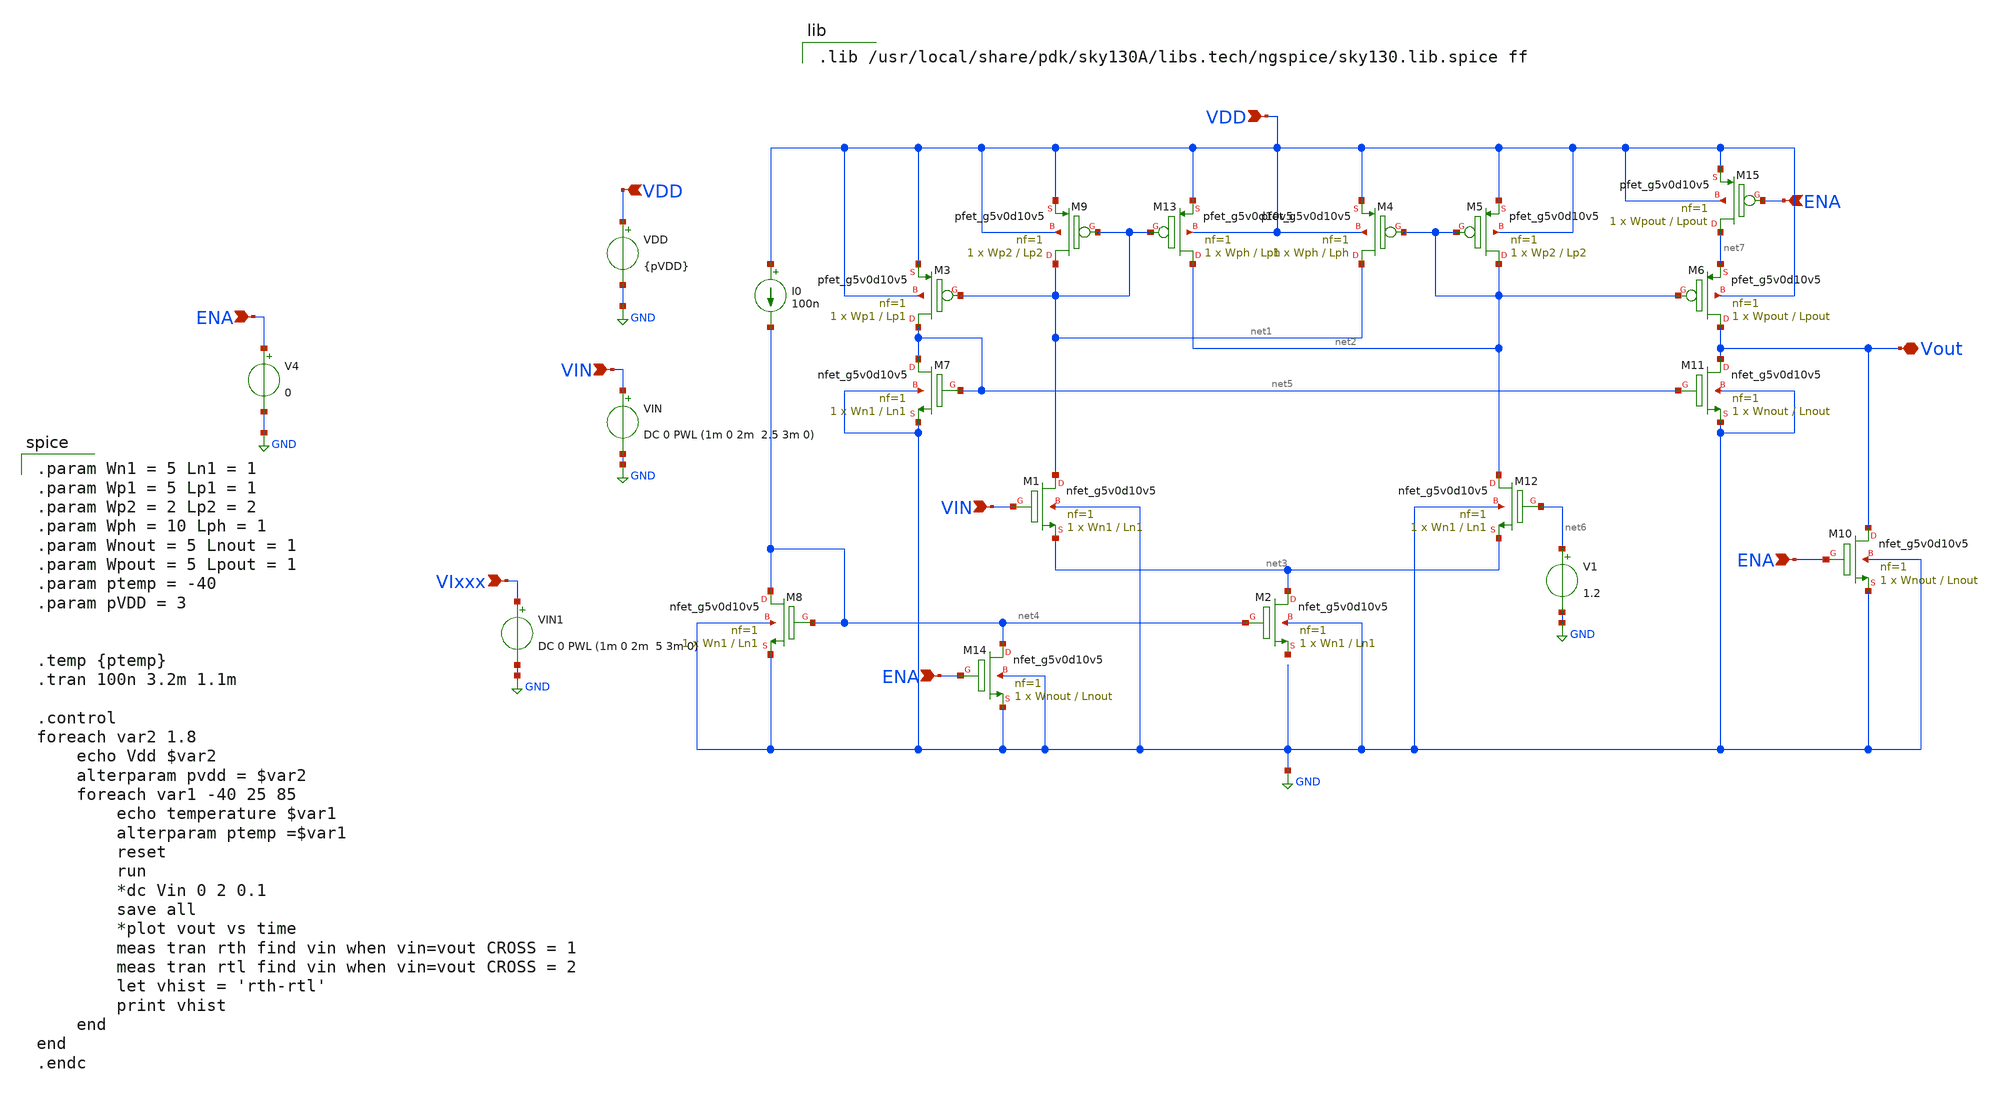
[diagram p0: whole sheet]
** sch_path: xschem/Comparador_Digital_voltage.sch
**.subckt Comparador_Digital_voltage VDD VDD Vout VIN VIN ENA ENA VIxxx ENA ENA
*.ipin VDD
*.ipin VDD
*.iopin Vout
*.ipin VIN
*.ipin VIN
*.ipin ENA
*.ipin ENA
*.ipin VIxxx
*.ipin ENA
*.ipin ENA
V1 net6 GND 1.2
VDD VDD GND {pVDD}
VIN VIN GND DC 0 PWL (1m 0 2m 2.5 3m 0)
I0 VDD net4 100n
XM3 net5 net1 VDD VDD sky130_fd_pr__pfet_g5v0d10v5 L=Lp1 W=Wp1 nf=1 ad='int((nf+1)/2) * W/nf * 0.29'
+ as='int((nf+2)/2) * W/nf * 0.29' pd='2*int((nf+1)/2) * (W/nf + 0.29)' ps='2*int((nf+2)/2) * (W/nf + 0.29)'
+ nrd='0.29 / W' nrs='0.29 / W' sa=0 sb=0 sd=0 mult=1 m=1
XM9 net1 net1 VDD VDD sky130_fd_pr__pfet_g5v0d10v5 L=Lp2 W=Wp2 nf=1 ad='int((nf+1)/2) * W/nf * 0.29'
+ as='int((nf+2)/2) * W/nf * 0.29' pd='2*int((nf+1)/2) * (W/nf + 0.29)' ps='2*int((nf+2)/2) * (W/nf + 0.29)'
+ nrd='0.29 / W' nrs='0.29 / W' sa=0 sb=0 sd=0 mult=1 m=1
XM13 net2 net1 VDD VDD sky130_fd_pr__pfet_g5v0d10v5 L=Lph W=Wph nf=1 ad='int((nf+1)/2) * W/nf * 0.29'
+ as='int((nf+2)/2) * W/nf * 0.29' pd='2*int((nf+1)/2) * (W/nf + 0.29)' ps='2*int((nf+2)/2) * (W/nf + 0.29)'
+ nrd='0.29 / W' nrs='0.29 / W' sa=0 sb=0 sd=0 mult=1 m=1
XM4 net1 net2 VDD VDD sky130_fd_pr__pfet_g5v0d10v5 L=Lph W=Wph nf=1 ad='int((nf+1)/2) * W/nf * 0.29'
+ as='int((nf+2)/2) * W/nf * 0.29' pd='2*int((nf+1)/2) * (W/nf + 0.29)' ps='2*int((nf+2)/2) * (W/nf + 0.29)'
+ nrd='0.29 / W' nrs='0.29 / W' sa=0 sb=0 sd=0 mult=1 m=1
XM5 net2 net2 VDD VDD sky130_fd_pr__pfet_g5v0d10v5 L=Lp2 W=Wp2 nf=1 ad='int((nf+1)/2) * W/nf * 0.29'
+ as='int((nf+2)/2) * W/nf * 0.29' pd='2*int((nf+1)/2) * (W/nf + 0.29)' ps='2*int((nf+2)/2) * (W/nf + 0.29)'
+ nrd='0.29 / W' nrs='0.29 / W' sa=0 sb=0 sd=0 mult=1 m=1
XM6 Vout net2 net7 VDD sky130_fd_pr__pfet_g5v0d10v5 L=Lpout W=Wpout nf=1 ad='int((nf+1)/2) * W/nf * 0.29'
+ as='int((nf+2)/2) * W/nf * 0.29' pd='2*int((nf+1)/2) * (W/nf + 0.29)' ps='2*int((nf+2)/2) * (W/nf + 0.29)'
+ nrd='0.29 / W' nrs='0.29 / W' sa=0 sb=0 sd=0 mult=1 m=1
XM11 Vout net5 GND GND sky130_fd_pr__nfet_g5v0d10v5 L=Lnout W=Wnout nf=1 ad='int((nf+1)/2) * W/nf * 0.29'
+ as='int((nf+2)/2) * W/nf * 0.29' pd='2*int((nf+1)/2) * (W/nf + 0.29)' ps='2*int((nf+2)/2) * (W/nf + 0.29)'
+ nrd='0.29 / W' nrs='0.29 / W' sa=0 sb=0 sd=0 mult=1 m=1
XM12 net2 net6 net3 GND sky130_fd_pr__nfet_g5v0d10v5 L=Ln1 W=Wn1 nf=1 ad='int((nf+1)/2) * W/nf * 0.29'
+ as='int((nf+2)/2) * W/nf * 0.29' pd='2*int((nf+1)/2) * (W/nf + 0.29)' ps='2*int((nf+2)/2) * (W/nf + 0.29)'
+ nrd='0.29 / W' nrs='0.29 / W' sa=0 sb=0 sd=0 mult=1 m=1
XM2 net3 net4 net8 GND sky130_fd_pr__nfet_g5v0d10v5 L=Ln1 W=Wn1 nf=1 ad='int((nf+1)/2) * W/nf * 0.29'
+ as='int((nf+2)/2) * W/nf * 0.29' pd='2*int((nf+1)/2) * (W/nf + 0.29)' ps='2*int((nf+2)/2) * (W/nf + 0.29)'
+ nrd='0.29 / W' nrs='0.29 / W' sa=0 sb=0 sd=0 mult=1 m=1
XM1 net1 VIN net3 GND sky130_fd_pr__nfet_g5v0d10v5 L=Ln1 W=Wn1 nf=1 ad='int((nf+1)/2) * W/nf * 0.29'
+ as='int((nf+2)/2) * W/nf * 0.29' pd='2*int((nf+1)/2) * (W/nf + 0.29)' ps='2*int((nf+2)/2) * (W/nf + 0.29)'
+ nrd='0.29 / W' nrs='0.29 / W' sa=0 sb=0 sd=0 mult=1 m=1
XM7 net5 net5 GND GND sky130_fd_pr__nfet_g5v0d10v5 L=Ln1 W=Wn1 nf=1 ad='int((nf+1)/2) * W/nf * 0.29'
+ as='int((nf+2)/2) * W/nf * 0.29' pd='2*int((nf+1)/2) * (W/nf + 0.29)' ps='2*int((nf+2)/2) * (W/nf + 0.29)'
+ nrd='0.29 / W' nrs='0.29 / W' sa=0 sb=0 sd=0 mult=1 m=1
XM8 net4 net4 GND GND sky130_fd_pr__nfet_g5v0d10v5 L=Ln1 W=Wn1 nf=1 ad='int((nf+1)/2) * W/nf * 0.29'
+ as='int((nf+2)/2) * W/nf * 0.29' pd='2*int((nf+1)/2) * (W/nf + 0.29)' ps='2*int((nf+2)/2) * (W/nf + 0.29)'
+ nrd='0.29 / W' nrs='0.29 / W' sa=0 sb=0 sd=0 mult=1 m=1
XM10 Vout ENA GND GND sky130_fd_pr__nfet_g5v0d10v5 L=Lnout W=Wnout nf=1 ad='int((nf+1)/2) * W/nf * 0.29'
+ as='int((nf+2)/2) * W/nf * 0.29' pd='2*int((nf+1)/2) * (W/nf + 0.29)' ps='2*int((nf+2)/2) * (W/nf + 0.29)'
+ nrd='0.29 / W' nrs='0.29 / W' sa=0 sb=0 sd=0 mult=1 m=1
XM14 net4 ENA GND GND sky130_fd_pr__nfet_g5v0d10v5 L=Lnout W=Wnout nf=1 ad='int((nf+1)/2) * W/nf * 0.29'
+ as='int((nf+2)/2) * W/nf * 0.29' pd='2*int((nf+1)/2) * (W/nf + 0.29)' ps='2*int((nf+2)/2) * (W/nf + 0.29)'
+ nrd='0.29 / W' nrs='0.29 / W' sa=0 sb=0 sd=0 mult=1 m=1
V4 ENA GND 0
VIN1 VIxxx GND DC 0 PWL (1m 0 2m 5 3m 0)
XM15 net7 ENA VDD VDD sky130_fd_pr__pfet_g5v0d10v5 L=Lpout W=Wpout nf=1 ad='int((nf+1)/2) * W/nf * 0.29'
+ as='int((nf+2)/2) * W/nf * 0.29' pd='2*int((nf+1)/2) * (W/nf + 0.29)' ps='2*int((nf+2)/2) * (W/nf + 0.29)'
+ nrd='0.29 / W' nrs='0.29 / W' sa=0 sb=0 sd=0 mult=1 m=1
**** begin user architecture code

.param Wn1 = 5 Ln1 = 1
.param Wp1 = 5 Lp1 = 1
.param Wp2 = 2 Lp2 = 2
.param Wph = 10 Lph = 1
.param Wnout = 5 Lnout = 1
.param Wpout = 5 Lpout = 1
.param ptemp = -40
.param pVDD = 3


.temp {ptemp}
.tran 100n 3.2m 1.1m

.control
foreach var2 1.8
	echo Vdd $var2
	alterparam pvdd = $var2
	foreach var1 -40 25 85
		echo temperature $var1
		alterparam ptemp =$var1
		reset
		run
		*dc Vin 0 2 0.1
		save all
		*plot vout vs time
		meas tran rth find vin when vin=vout CROSS = 1
		meas tran rtl find vin when vin=vout CROSS = 2
		let vhist = 'rth-rtl'
		print vhist
	end
end
.endc


.lib /usr/local/share/pdk/sky130A/libs.tech/ngspice/sky130.lib.spice ff

**** end user architecture code
**.ends
.GLOBAL GND
.end
